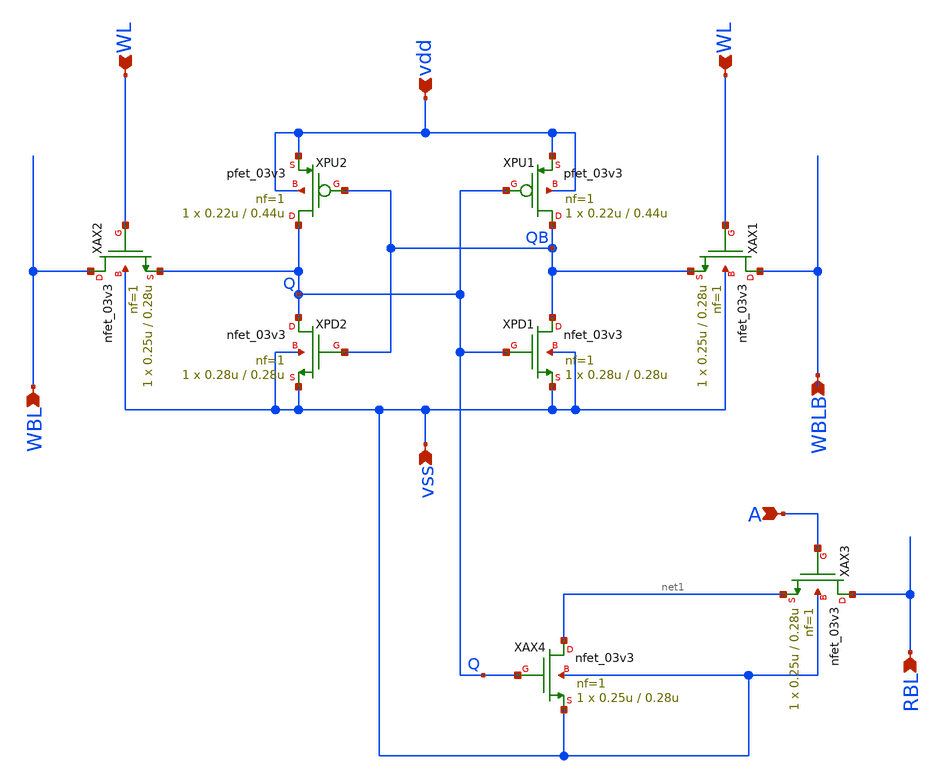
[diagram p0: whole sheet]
** sch_path: analog/designs/8T_03v3.sch
**.subckt 8T_03v3 vss vdd WL WL WBL WBLB A RBL
*.ipin vss
*.ipin vdd
*.ipin WL
*.ipin WL
*.ipin WBL
*.ipin WBLB
*.ipin A
*.ipin RBL
XPD1 QB Q vss vss nfet_03v3 L=0.28u W=0.28u nf=1 ad='int((nf+1)/2) * W/nf * 0.18u' as='int((nf+2)/2) * W/nf * 0.18u'
+ pd='2*int((nf+1)/2) * (W/nf + 0.18u)' ps='2*int((nf+2)/2) * (W/nf + 0.18u)' nrd='0.18u / W' nrs='0.18u / W'
+ sa=0 sb=0 sd=0 m=1
XPU1 QB Q vdd vdd pfet_03v3 L=0.44u W=0.22u nf=1 ad='int((nf+1)/2) * W/nf * 0.18u' as='int((nf+2)/2) * W/nf * 0.18u'
+ pd='2*int((nf+1)/2) * (W/nf + 0.18u)' ps='2*int((nf+2)/2) * (W/nf + 0.18u)' nrd='0.18u / W' nrs='0.18u / W'
+ sa=0 sb=0 sd=0 m=1
XAX1 WBLB WL QB vss nfet_03v3 L=0.28u W=0.25u nf=1 ad='int((nf+1)/2) * W/nf * 0.18u' as='int((nf+2)/2) * W/nf * 0.18u'
+ pd='2*int((nf+1)/2) * (W/nf + 0.18u)' ps='2*int((nf+2)/2) * (W/nf + 0.18u)' nrd='0.18u / W' nrs='0.18u / W'
+ sa=0 sb=0 sd=0 m=1
XPD2 Q QB vss vss nfet_03v3 L=0.28u W=0.28u nf=1 ad='int((nf+1)/2) * W/nf * 0.18u' as='int((nf+2)/2) * W/nf * 0.18u'
+ pd='2*int((nf+1)/2) * (W/nf + 0.18u)' ps='2*int((nf+2)/2) * (W/nf + 0.18u)' nrd='0.18u / W' nrs='0.18u / W'
+ sa=0 sb=0 sd=0 m=1
XPU2 Q QB vdd vdd pfet_03v3 L=0.44u W=0.22u nf=1 ad='int((nf+1)/2) * W/nf * 0.18u' as='int((nf+2)/2) * W/nf * 0.18u'
+ pd='2*int((nf+1)/2) * (W/nf + 0.18u)' ps='2*int((nf+2)/2) * (W/nf + 0.18u)' nrd='0.18u / W' nrs='0.18u / W'
+ sa=0 sb=0 sd=0 m=1
XAX2 WBL WL Q vss nfet_03v3 L=0.28u W=0.25u nf=1 ad='int((nf+1)/2) * W/nf * 0.18u' as='int((nf+2)/2) * W/nf * 0.18u'
+ pd='2*int((nf+1)/2) * (W/nf + 0.18u)' ps='2*int((nf+2)/2) * (W/nf + 0.18u)' nrd='0.18u / W' nrs='0.18u / W'
+ sa=0 sb=0 sd=0 m=1
XAX4 net1 Q vss vss nfet_03v3 L=0.28u W=0.25u nf=1 ad='int((nf+1)/2) * W/nf * 0.18u' as='int((nf+2)/2) * W/nf * 0.18u'
+ pd='2*int((nf+1)/2) * (W/nf + 0.18u)' ps='2*int((nf+2)/2) * (W/nf + 0.18u)' nrd='0.18u / W' nrs='0.18u / W'
+ sa=0 sb=0 sd=0 m=1
XAX3 RBL A net1 vss nfet_03v3 L=0.28u W=0.25u nf=1 ad='int((nf+1)/2) * W/nf * 0.18u' as='int((nf+2)/2) * W/nf * 0.18u'
+ pd='2*int((nf+1)/2) * (W/nf + 0.18u)' ps='2*int((nf+2)/2) * (W/nf + 0.18u)' nrd='0.18u / W' nrs='0.18u / W'
+ sa=0 sb=0 sd=0 m=1
**.ends
.end
